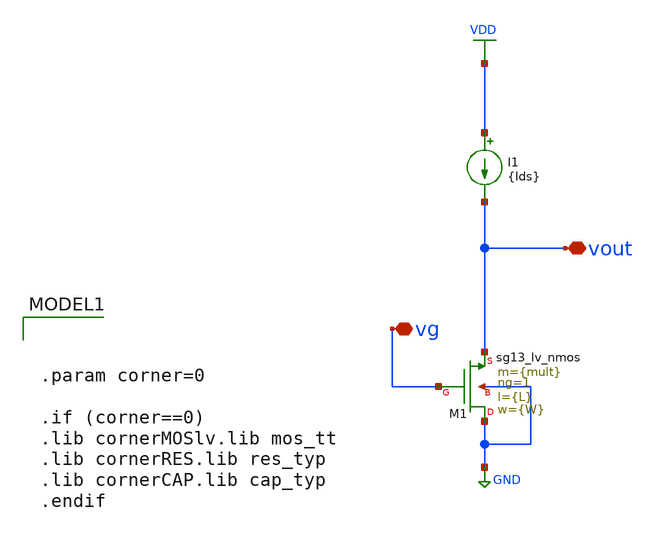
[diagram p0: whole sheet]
** sch_path: Tarea_1/xschem/cs_amp_full_IPD413HW1.sch
**.subckt cs_amp_full_IPD413HW1 vg vout
*.iopin vg
*.iopin vout
I1 VDD vout {Ids}
XM1 GND vg vout GND sg13_lv_nmos w={W} l={L} ng=1 m={mult} mm_ok=1
**** begin user architecture code


.param corner=0

.if (corner==0)
.lib cornerMOSlv.lib mos_tt
.lib cornerRES.lib res_typ
.lib cornerCAP.lib cap_typ
.endif



.option wnflag=1
.param gm    = {3.1415*1.1m}
.param gm_id = 13
.param Ids   = {gm/gm_id}
.param L     = 0.13u
.param W     = 3.13u
.param mult  = 10

vsup VDD 0 1.8
vin vg 0 dc=0.45 ac=1

cload vout 0 5p

.control
save all
op
save @n.xm1.nsg13_lv_nmos[gm]
save @n.xm1.nsg13_lv_nmos[ids]
save @n.xm1.nsg13_lv_nmos[gds]
save @n.xm1.nsg13_lv_nmos[ib]

*dc vin -0.01 0.01 0.001
dc vin 0.45 0.45 0.001

let gdsn = @n.xm1.nsg13_lv_nmos[gds]
let gmn = @n.xm1.nsg13_lv_nmos[gm]
let vthn = @n.xm1.nsg13_lv_nmos[vth]
let idn = @n.xm1.nsg13_lv_nmos[ids]
let ao = gmn / gdsn

print Ao

ac dec 100 1 1T
plot vdb(vout)
meas ac GBW when vdb(vout)=0
meas ac DCG find vdb(vout) at=1]]
wrdata cs_amp_bode.raw vdb(vout)
.endc

**** end user architecture code
**.ends
.GLOBAL GND
.GLOBAL VDD
.end
